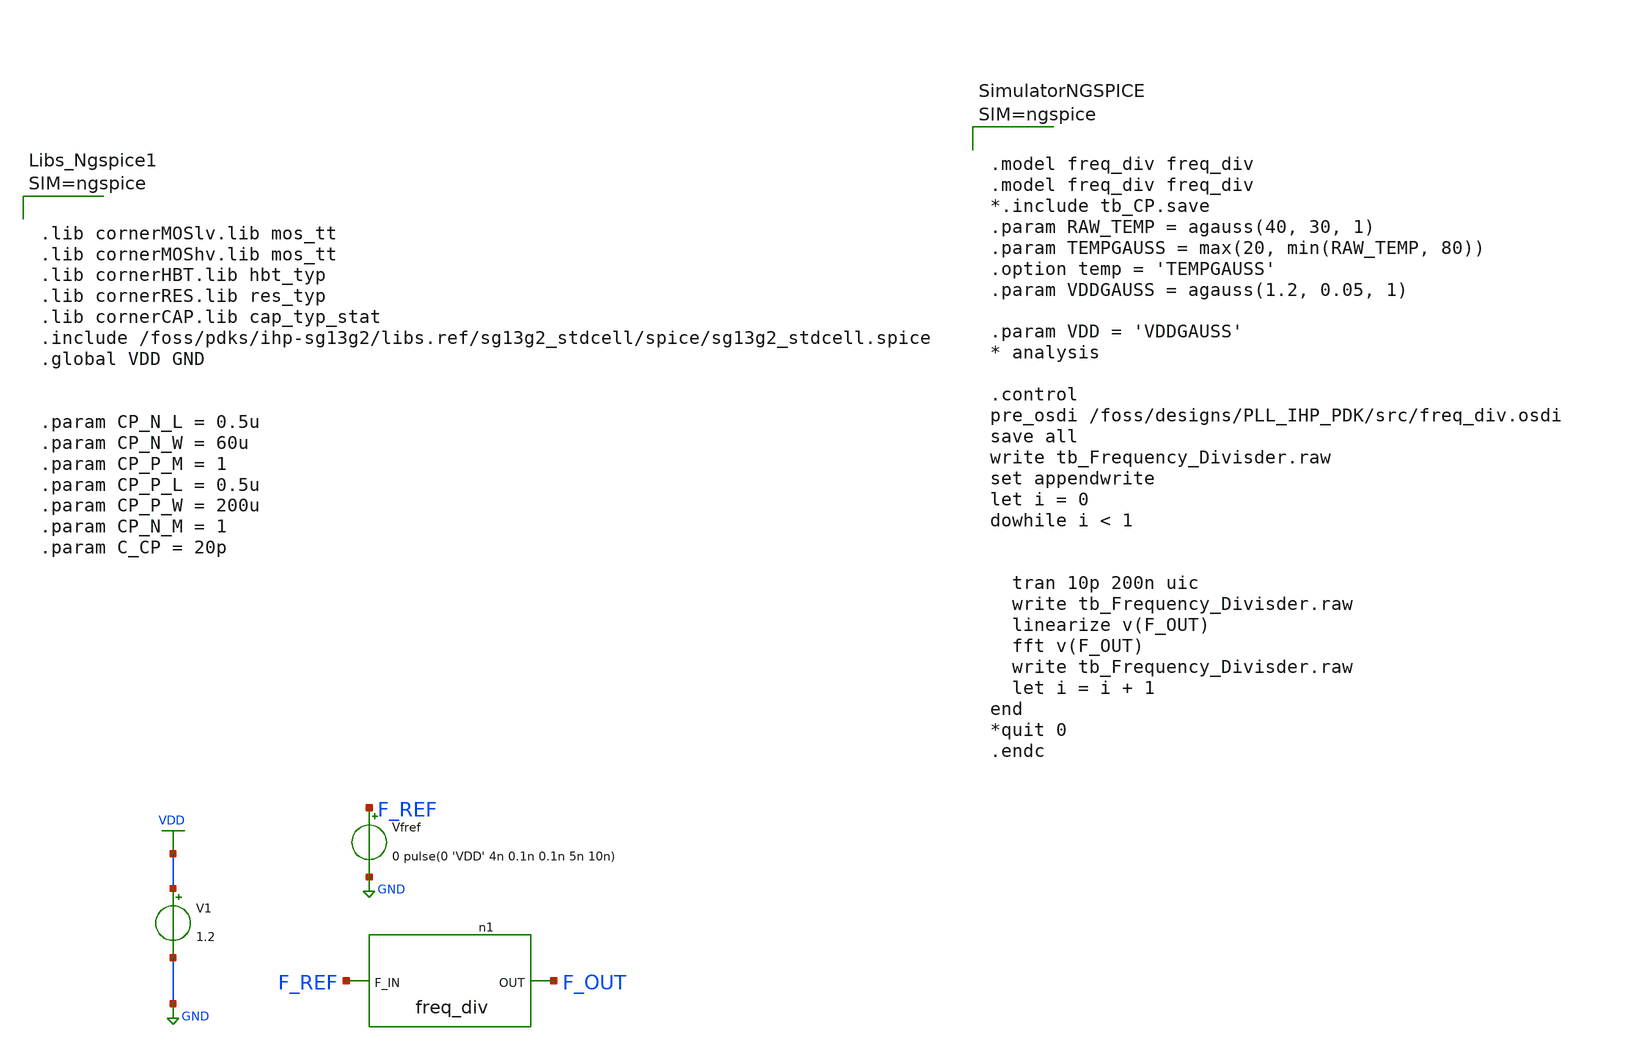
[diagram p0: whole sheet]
** sch_path: tb/tb_Frequency_Divider.sch
**.subckt tb_Frequency_Divider
V1 VDD GND 1.2
Vfref F_REF GND 0 pulse(0 'VDD' 4n 0.1n 0.1n 5n 10n)
n1 F_OUT F_REF freq_div
**** begin user architecture code



.model freq_div freq_div
.model freq_div freq_div
*.include tb_CP.save
.param RAW_TEMP = agauss(40, 30, 1)
.param TEMPGAUSS = max(20, min(RAW_TEMP, 80))
.option temp = 'TEMPGAUSS'
.param VDDGAUSS = agauss(1.2, 0.05, 1)

.param VDD = 'VDDGAUSS'
* analysis

.control
pre_osdi /foss/designs/PLL_IHP_PDK/src/freq_div.osdi
save all
write tb_Frequency_Divisder.raw
set appendwrite
let i = 0
dowhile i < 1


  tran 10p 200n uic
  write tb_Frequency_Divisder.raw
  linearize v(F_OUT)
  fft v(F_OUT)
  write tb_Frequency_Divisder.raw
  let i = i + 1
end
*quit 0
.endc






.lib cornerMOSlv.lib mos_tt
.lib cornerMOShv.lib mos_tt
.lib cornerHBT.lib hbt_typ
.lib cornerRES.lib res_typ
.lib cornerCAP.lib cap_typ_stat
.include /foss/pdks/ihp-sg13g2/libs.ref/sg13g2_stdcell/spice/sg13g2_stdcell.spice
.global VDD GND


.param CP_N_L = 0.5u
.param CP_N_W = 60u
.param CP_P_M = 1
.param CP_P_L = 0.5u
.param CP_P_W = 200u
.param CP_N_M = 1
.param C_CP = 20p



**** end user architecture code
**.ends
.GLOBAL GND
.GLOBAL VDD
.end
